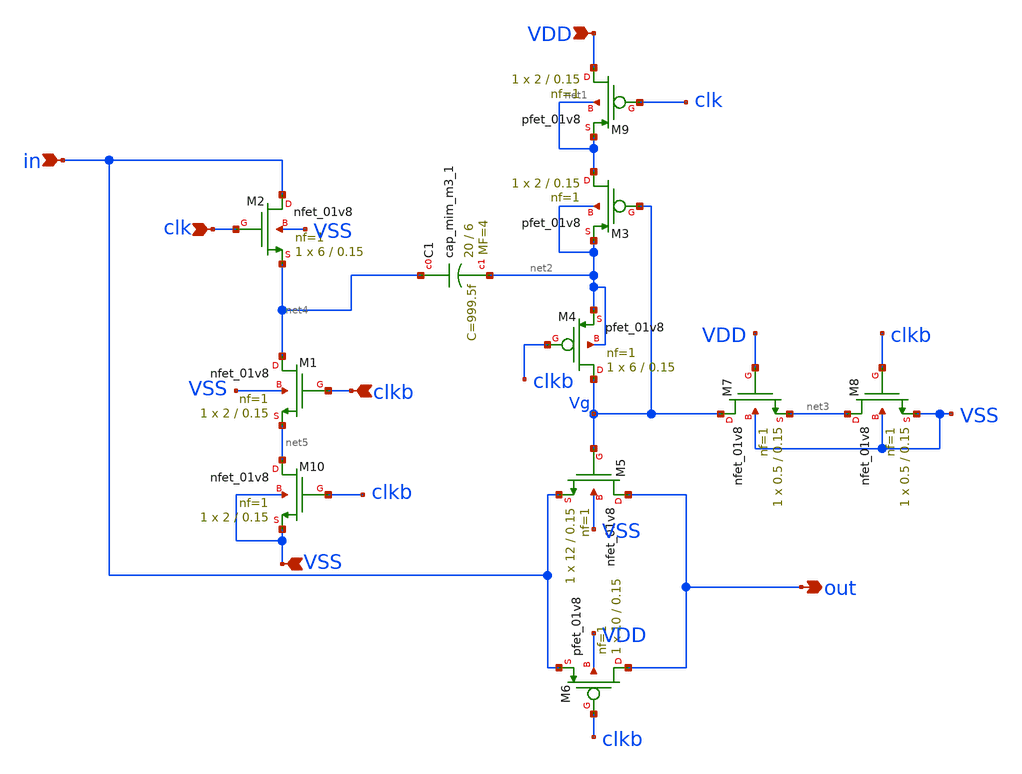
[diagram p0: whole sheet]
** sch_path: SampleHold/Boostrapped_switch_v2.sch
**.subckt Boostrapped_switch_v2 in out VSS VDD clkb clk
*.ipin in
*.opin out
*.ipin VSS
*.ipin VDD
*.ipin clkb
*.ipin clk
XM1 net4 clkb net5 VSS sky130_fd_pr__nfet_01v8 L=0.15 W=2 nf=1 ad='int((nf+1)/2) * W/nf * 0.29' as='int((nf+2)/2) * W/nf * 0.29'
+ pd='2*int((nf+1)/2) * (W/nf + 0.29)' ps='2*int((nf+2)/2) * (W/nf + 0.29)' nrd='0.29 / W' nrs='0.29 / W'
+ sa=0 sb=0 sd=0 mult=1 m=1
XM2 in clk net4 VSS sky130_fd_pr__nfet_01v8 L=0.15 W=6 nf=1 ad='int((nf+1)/2) * W/nf * 0.29' as='int((nf+2)/2) * W/nf * 0.29'
+ pd='2*int((nf+1)/2) * (W/nf + 0.29)' ps='2*int((nf+2)/2) * (W/nf + 0.29)' nrd='0.29 / W' nrs='0.29 / W'
+ sa=0 sb=0 sd=0 mult=1 m=1
XM3 net1 Vg net2 net2 sky130_fd_pr__pfet_01v8 L=0.15 W=2 nf=1 ad='int((nf+1)/2) * W/nf * 0.29' as='int((nf+2)/2) * W/nf * 0.29'
+ pd='2*int((nf+1)/2) * (W/nf + 0.29)' ps='2*int((nf+2)/2) * (W/nf + 0.29)' nrd='0.29 / W' nrs='0.29 / W'
+ sa=0 sb=0 sd=0 mult=1 m=1
XM4 Vg clkb net2 net2 sky130_fd_pr__pfet_01v8 L=0.15 W=6 nf=1 ad='int((nf+1)/2) * W/nf * 0.29' as='int((nf+2)/2) * W/nf * 0.29'
+ pd='2*int((nf+1)/2) * (W/nf + 0.29)' ps='2*int((nf+2)/2) * (W/nf + 0.29)' nrd='0.29 / W' nrs='0.29 / W'
+ sa=0 sb=0 sd=0 mult=1 m=1
XM5 out Vg in VSS sky130_fd_pr__nfet_01v8 L=0.15 W=12 nf=1 ad='int((nf+1)/2) * W/nf * 0.29' as='int((nf+2)/2) * W/nf * 0.29'
+ pd='2*int((nf+1)/2) * (W/nf + 0.29)' ps='2*int((nf+2)/2) * (W/nf + 0.29)' nrd='0.29 / W' nrs='0.29 / W'
+ sa=0 sb=0 sd=0 mult=1 m=1
XM6 out clkb in VDD sky130_fd_pr__pfet_01v8 L=0.15 W=10 nf=1 ad='int((nf+1)/2) * W/nf * 0.29' as='int((nf+2)/2) * W/nf * 0.29'
+ pd='2*int((nf+1)/2) * (W/nf + 0.29)' ps='2*int((nf+2)/2) * (W/nf + 0.29)' nrd='0.29 / W' nrs='0.29 / W'
+ sa=0 sb=0 sd=0 mult=1 m=1
XM7 Vg VDD net3 VSS sky130_fd_pr__nfet_01v8 L=0.15 W=0.5 nf=1 ad='int((nf+1)/2) * W/nf * 0.29' as='int((nf+2)/2) * W/nf * 0.29'
+ pd='2*int((nf+1)/2) * (W/nf + 0.29)' ps='2*int((nf+2)/2) * (W/nf + 0.29)' nrd='0.29 / W' nrs='0.29 / W'
+ sa=0 sb=0 sd=0 mult=1 m=1
XM8 net3 clkb VSS VSS sky130_fd_pr__nfet_01v8 L=0.15 W=0.5 nf=1 ad='int((nf+1)/2) * W/nf * 0.29' as='int((nf+2)/2) * W/nf * 0.29'
+ pd='2*int((nf+1)/2) * (W/nf + 0.29)' ps='2*int((nf+2)/2) * (W/nf + 0.29)' nrd='0.29 / W' nrs='0.29 / W'
+ sa=0 sb=0 sd=0 mult=1 m=1
XC1 net4 net2 sky130_fd_pr__cap_mim_m3_1 W=20 L=6 MF=4 m=4
XM9 VDD clk net1 net1 sky130_fd_pr__pfet_01v8 L=0.15 W=2 nf=1 ad='int((nf+1)/2) * W/nf * 0.29' as='int((nf+2)/2) * W/nf * 0.29'
+ pd='2*int((nf+1)/2) * (W/nf + 0.29)' ps='2*int((nf+2)/2) * (W/nf + 0.29)' nrd='0.29 / W' nrs='0.29 / W'
+ sa=0 sb=0 sd=0 mult=1 m=1
XM10 net5 clkb VSS VSS sky130_fd_pr__nfet_01v8 L=0.15 W=2 nf=1 ad='int((nf+1)/2) * W/nf * 0.29' as='int((nf+2)/2) * W/nf * 0.29'
+ pd='2*int((nf+1)/2) * (W/nf + 0.29)' ps='2*int((nf+2)/2) * (W/nf + 0.29)' nrd='0.29 / W' nrs='0.29 / W'
+ sa=0 sb=0 sd=0 mult=1 m=1
**.ends
.end
